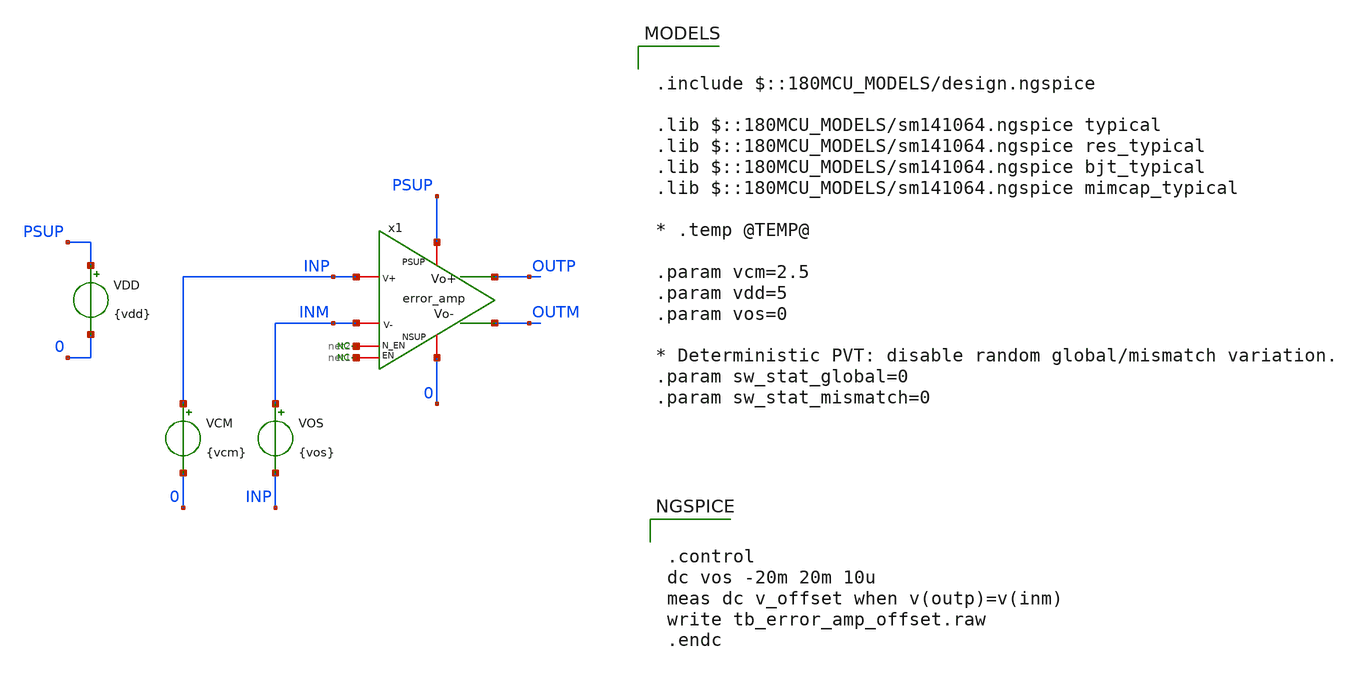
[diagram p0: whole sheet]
** sch_path: xschem/blocks/error_amp/tb_error_amp_offset.sch
**.subckt tb_error_amp_offset
VDD PSUP 0 {vdd}
VCM INP 0 {vcm}
* noconn #net1
* noconn #net2
VOS INM INP {vos}
x1 PSUP INP INM net2 0 net1 OUTM OUTP error_amp
**** begin user architecture code


.control
dc vos -20m 20m 10u
meas dc v_offset when v(outp)=v(inm)
write tb_error_amp_offset.raw
.endc



.include $::180MCU_MODELS/design.ngspice

.lib $::180MCU_MODELS/sm141064.ngspice typical
.lib $::180MCU_MODELS/sm141064.ngspice res_typical
.lib $::180MCU_MODELS/sm141064.ngspice bjt_typical
.lib $::180MCU_MODELS/sm141064.ngspice mimcap_typical

* .temp @TEMP@

.param vcm=2.5
.param vdd=5
.param vos=0

* Deterministic PVT: disable random global/mismatch variation.
.param sw_stat_global=0
.param sw_stat_mismatch=0


**** end user architecture code
**.ends

* expanding   symbol:  blocks/error_amp/error_amp.sym # of pins=8
** sym_path: xschem/blocks/error_amp/error_amp.sym
** sch_path: xschem/blocks/error_amp/error_amp.sch
.subckt error_amp PSUP V+ V- N_EN NSUP EN Vo- Vo+
*.ipin PSUP
*.ipin NSUP
*.ipin N_EN
*.ipin EN
*.ipin V+
*.ipin V-
*.opin Vo-
*.opin Vo+
XM5 AA1 vb1 PSUP PSUP pfet_06v0 L=4u W=2u nf=4 ad='int((nf+1)/2) * W/nf * 0.18u' as='int((nf+2)/2) * W/nf * 0.18u'
+ pd='2*int((nf+1)/2) * (W/nf + 0.18u)' ps='2*int((nf+2)/2) * (W/nf + 0.18u)' nrd='0.18u / W' nrs='0.18u / W'
+ sa=0 sb=0 sd=0 m=2
XM6 AA2 vb1 PSUP PSUP pfet_06v0 L=4u W=2u nf=4 ad='int((nf+1)/2) * W/nf * 0.18u' as='int((nf+2)/2) * W/nf * 0.18u'
+ pd='2*int((nf+1)/2) * (W/nf + 0.18u)' ps='2*int((nf+2)/2) * (W/nf + 0.18u)' nrd='0.18u / W' nrs='0.18u / W'
+ sa=0 sb=0 sd=0 m=2
* noconn N_EN
* noconn EN
XM1 AA4 V- AA5 NSUP nfet_06v0 L=2u W=4u nf=5 ad='int((nf+1)/2) * W/nf * 0.18u' as='int((nf+2)/2) * W/nf * 0.18u'
+ pd='2*int((nf+1)/2) * (W/nf + 0.18u)' ps='2*int((nf+2)/2) * (W/nf + 0.18u)' nrd='0.18u / W' nrs='0.18u / W'
+ sa=0 sb=0 sd=0 m=4
XM4 mirror mirror NSUP NSUP nfet_06v0 L=4u W=2u nf=2 ad='int((nf+1)/2) * W/nf * 0.18u' as='int((nf+2)/2) * W/nf * 0.18u'
+ pd='2*int((nf+1)/2) * (W/nf + 0.18u)' ps='2*int((nf+2)/2) * (W/nf + 0.18u)' nrd='0.18u / W' nrs='0.18u / W'
+ sa=0 sb=0 sd=0 m=1
I0 vb2 mirror 1u
XM7 AA5 mirror NSUP NSUP nfet_06v0 L=4u W=2u nf=4 ad='int((nf+1)/2) * W/nf * 0.18u' as='int((nf+2)/2) * W/nf * 0.18u'
+ pd='2*int((nf+1)/2) * (W/nf + 0.18u)' ps='2*int((nf+2)/2) * (W/nf + 0.18u)' nrd='0.18u / W' nrs='0.18u / W'
+ sa=0 sb=0 sd=0 m=2
XM3 vb1 vb1 PSUP PSUP pfet_06v0 L=4u W=2u nf=1 ad='int((nf+1)/2) * W/nf * 0.18u' as='int((nf+2)/2) * W/nf * 0.18u'
+ pd='2*int((nf+1)/2) * (W/nf + 0.18u)' ps='2*int((nf+2)/2) * (W/nf + 0.18u)' nrd='0.18u / W' nrs='0.18u / W'
+ sa=0 sb=0 sd=0 m=2
XM8 Vo+ vb2 AA1 AA1 pfet_06v0 L=4u W=2u nf=4 ad='int((nf+1)/2) * W/nf * 0.18u' as='int((nf+2)/2) * W/nf * 0.18u'
+ pd='2*int((nf+1)/2) * (W/nf + 0.18u)' ps='2*int((nf+2)/2) * (W/nf + 0.18u)' nrd='0.18u / W' nrs='0.18u / W'
+ sa=0 sb=0 sd=0 m=2
XM9 Vo- vb2 AA2 AA2 pfet_06v0 L=4u W=2u nf=4 ad='int((nf+1)/2) * W/nf * 0.18u' as='int((nf+2)/2) * W/nf * 0.18u'
+ pd='2*int((nf+1)/2) * (W/nf + 0.18u)' ps='2*int((nf+2)/2) * (W/nf + 0.18u)' nrd='0.18u / W' nrs='0.18u / W'
+ sa=0 sb=0 sd=0 m=2
XM10 vb2 vb2 vb1 vb1 pfet_06v0 L=4u W=2u nf=1 ad='int((nf+1)/2) * W/nf * 0.18u' as='int((nf+2)/2) * W/nf * 0.18u'
+ pd='2*int((nf+1)/2) * (W/nf + 0.18u)' ps='2*int((nf+2)/2) * (W/nf + 0.18u)' nrd='0.18u / W' nrs='0.18u / W'
+ sa=0 sb=0 sd=0 m=2
XM2 AA3 V+ AA5 NSUP nfet_06v0 L=2u W=4u nf=5 ad='int((nf+1)/2) * W/nf * 0.18u' as='int((nf+2)/2) * W/nf * 0.18u'
+ pd='2*int((nf+1)/2) * (W/nf + 0.18u)' ps='2*int((nf+2)/2) * (W/nf + 0.18u)' nrd='0.18u / W' nrs='0.18u / W'
+ sa=0 sb=0 sd=0 m=4
XM11 Vo+ vb2 AA3 AA3 nfet_06v0 L=4u W=2u nf=4 ad='int((nf+1)/2) * W/nf * 0.18u' as='int((nf+2)/2) * W/nf * 0.18u'
+ pd='2*int((nf+1)/2) * (W/nf + 0.18u)' ps='2*int((nf+2)/2) * (W/nf + 0.18u)' nrd='0.18u / W' nrs='0.18u / W'
+ sa=0 sb=0 sd=0 m=2
XM12 Vo- vb2 AA4 AA4 nfet_06v0 L=4u W=2u nf=4 ad='int((nf+1)/2) * W/nf * 0.18u' as='int((nf+2)/2) * W/nf * 0.18u'
+ pd='2*int((nf+1)/2) * (W/nf + 0.18u)' ps='2*int((nf+2)/2) * (W/nf + 0.18u)' nrd='0.18u / W' nrs='0.18u / W'
+ sa=0 sb=0 sd=0 m=2
.ends

.end
